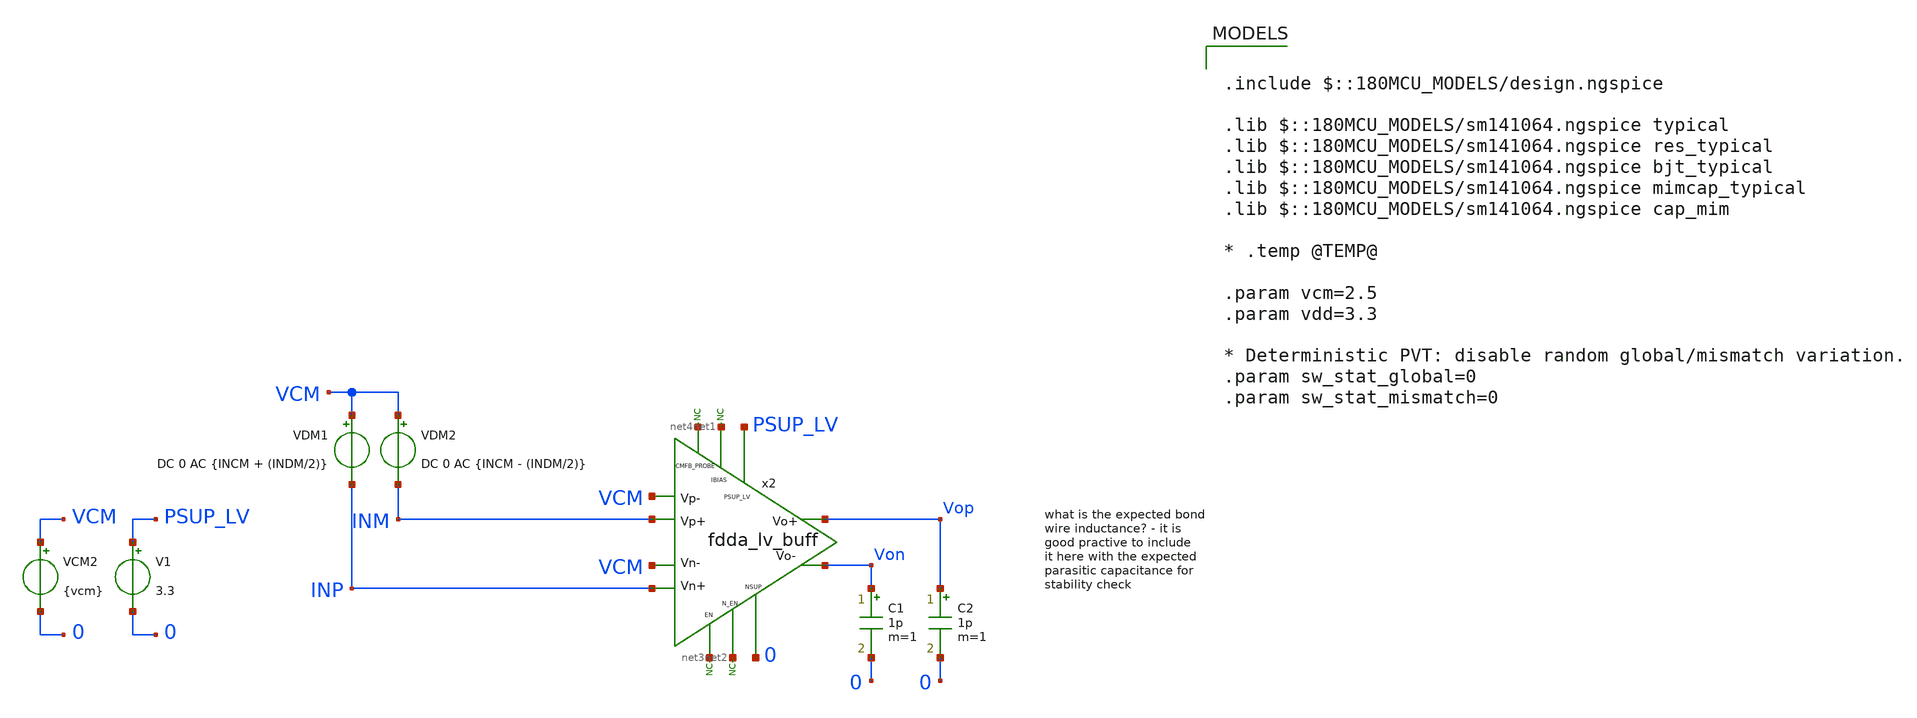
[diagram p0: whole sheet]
** sch_path: xschem/blocks/fdda_lv_buff/tb_fdda_lv_buff_cmrr.sch
**.subckt tb_fdda_lv_buff_cmrr
C1 Von 0 1p m=1
x2 PSUP_LV VCM VCM INP INM Vop Von net1 net2 net3 0 net4 fdda_lv_buff
* noconn #net1
* noconn #net3
* noconn #net2
V1 PSUP_LV 0 3.3
C2 Vop 0 1p m=1
VCM2 VCM 0 {vcm}
VDM2 VCM INM DC 0 AC {INCM - (INDM/2)}
VDM1 VCM INP DC 0 AC {INCM + (INDM/2)}
* noconn #net4
**** begin user architecture code

.include $::180MCU_MODELS/design.ngspice

.lib $::180MCU_MODELS/sm141064.ngspice typical
.lib $::180MCU_MODELS/sm141064.ngspice res_typical
.lib $::180MCU_MODELS/sm141064.ngspice bjt_typical
.lib $::180MCU_MODELS/sm141064.ngspice mimcap_typical
.lib $::180MCU_MODELS/sm141064.ngspice cap_mim

* .temp @TEMP@

.param vcm=2.5
.param vdd=3.3

* Deterministic PVT: disable random global/mismatch variation.
.param sw_stat_global=0
.param sw_stat_mismatch=0



.control
set units=degrees
save all

.param INCM=0
.param INDM=1

* ==================================================
* 1. Differential gain
* ==================================================

alterparam INCM=0
alterparam INDM=1
reset

ac dec 100 1 1G

let Vdi = v(INP) - v(INM)
let Vdo = v(Vop) - v(Von)
let Ad = Vdo / Vdi
let gain_diff_db = db(Ad)
let phase_diff_deg = cph(Ad)

meas ac UGF when gain_diff_db=0
meas ac phase_margin find phase_diff_deg when gain_diff_db=0

write tb_fdda_lv_buff_cmrr_aol.raw frequency v(Vop) v(Von) Vdo Ad gain_diff_db phase_diff_deg

* ==================================================
* 2. Common-mode gain
* ==================================================

alterparam INCM=1
alterparam INDM=0
reset

ac dec 100 1 1G

let Vci = (v(INP) + v(INM))/2
let Vco = v(Vop) - v(Von)
let Ac  = Vco/Vci

let gain_comm_db = db(Ac)
let phase_comm_deg = cph(Ac)

write tb_fdda_lv_buff_cmrr_acm.raw frequency v(Vop) v(Von) Vco Ac gain_comm_db phase_comm_deg

* ==================================================
* 3. CMRR
* ==================================================

.endc


**** end user architecture code
**.ends
.end
